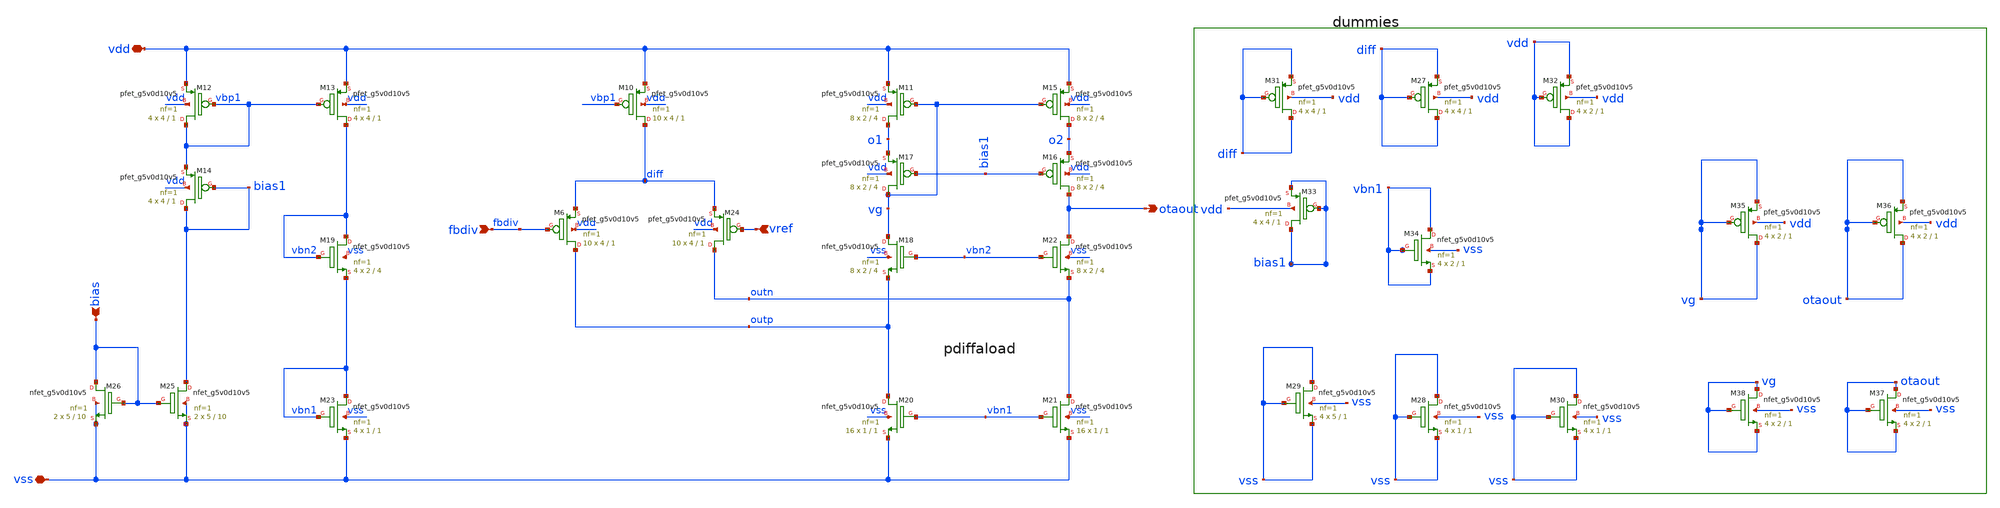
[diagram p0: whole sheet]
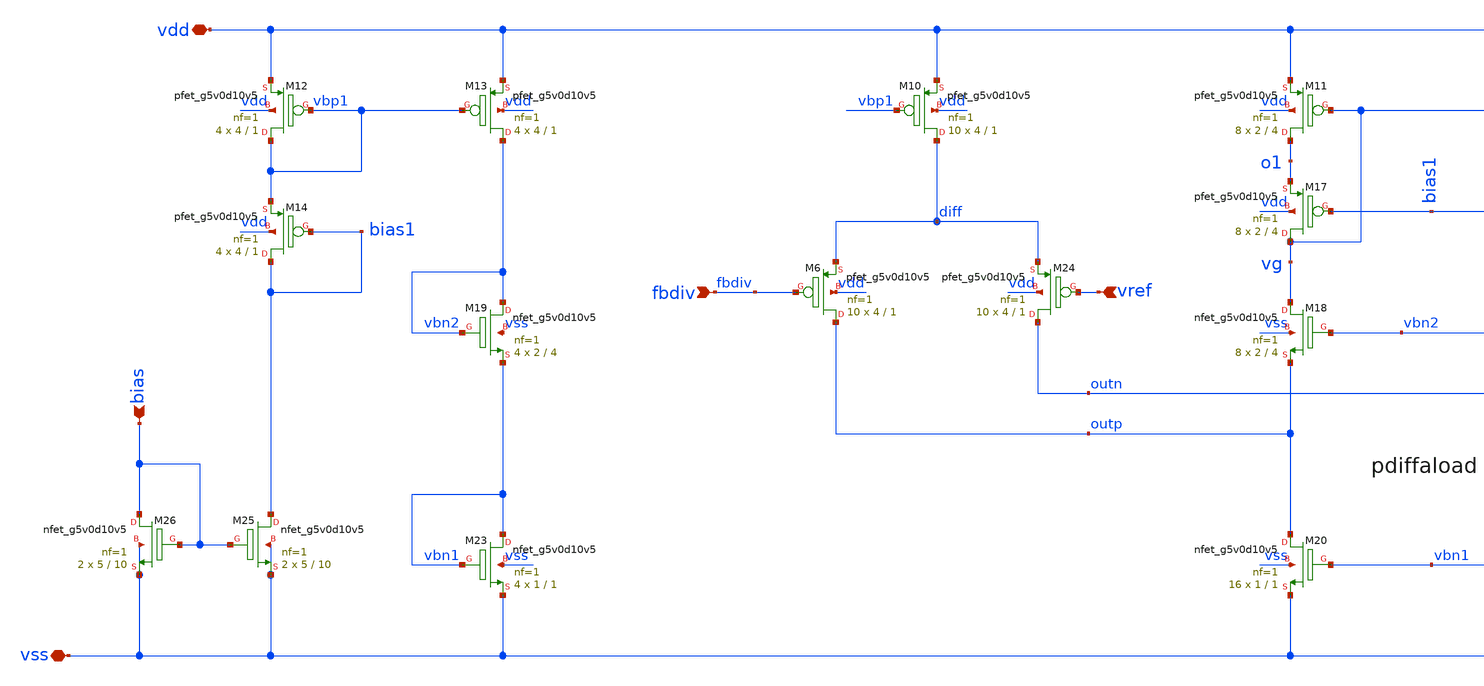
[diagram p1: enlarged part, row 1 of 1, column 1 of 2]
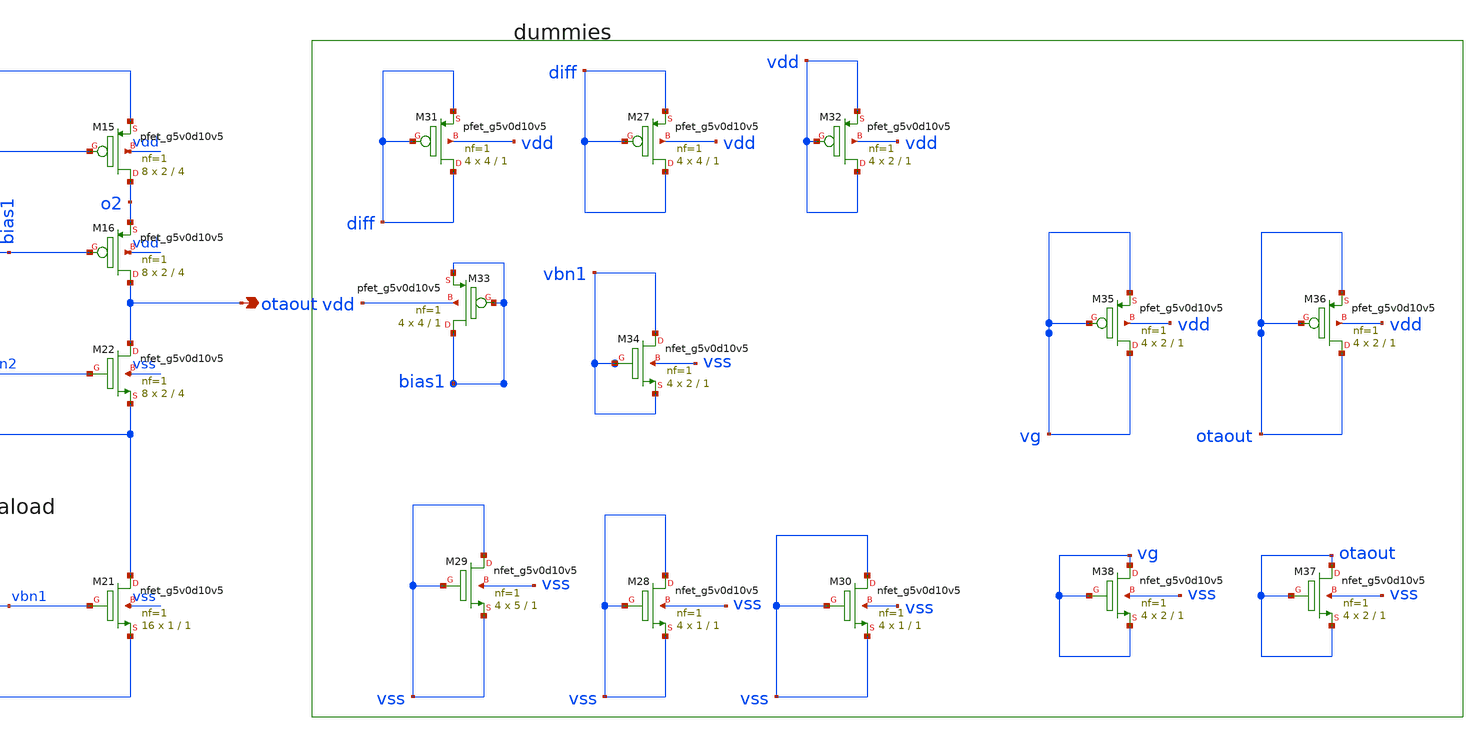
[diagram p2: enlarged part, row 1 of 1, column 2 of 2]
** sch_path: schematic/otaldox.sch
**.subckt otaldox vref bias vss vdd fbdiv otaout
*.ipin vref
*.ipin bias
*.iopin vss
*.iopin vdd
*.ipin fbdiv
*.opin otaout
XM12 vbp1 vbp1 vdd vdd sky130_fd_pr__pfet_g5v0d10v5 L=1 W=4 nf=1 ad='int((nf+1)/2) * W/nf * 0.29' as='int((nf+2)/2) * W/nf * 0.29'
+ pd='2*int((nf+1)/2) * (W/nf + 0.29)' ps='2*int((nf+2)/2) * (W/nf + 0.29)' nrd='0.29 / W' nrs='0.29 / W'
+ sa=0 sb=0 sd=0 mult=4 m=4
XM13 vbn2 vbp1 vdd vdd sky130_fd_pr__pfet_g5v0d10v5 L=1 W=4 nf=1 ad='int((nf+1)/2) * W/nf * 0.29' as='int((nf+2)/2) * W/nf * 0.29'
+ pd='2*int((nf+1)/2) * (W/nf + 0.29)' ps='2*int((nf+2)/2) * (W/nf + 0.29)' nrd='0.29 / W' nrs='0.29 / W'
+ sa=0 sb=0 sd=0 mult=4 m=4
XM14 bias1 bias1 vbp1 vdd sky130_fd_pr__pfet_g5v0d10v5 L=1 W=4 nf=1 ad='int((nf+1)/2) * W/nf * 0.29'
+ as='int((nf+2)/2) * W/nf * 0.29' pd='2*int((nf+1)/2) * (W/nf + 0.29)' ps='2*int((nf+2)/2) * (W/nf + 0.29)'
+ nrd='0.29 / W' nrs='0.29 / W' sa=0 sb=0 sd=0 mult=4 m=4
XM6 outp fbdiv diff vdd sky130_fd_pr__pfet_g5v0d10v5 L=1 W=4 nf=1 ad='int((nf+1)/2) * W/nf * 0.29' as='int((nf+2)/2) * W/nf * 0.29'
+ pd='2*int((nf+1)/2) * (W/nf + 0.29)' ps='2*int((nf+2)/2) * (W/nf + 0.29)' nrd='0.29 / W' nrs='0.29 / W'
+ sa=0 sb=0 sd=0 mult=10 m=10
XM10 diff vbp1 vdd vdd sky130_fd_pr__pfet_g5v0d10v5 L=1 W=4 nf=1 ad='int((nf+1)/2) * W/nf * 0.29' as='int((nf+2)/2) * W/nf * 0.29'
+ pd='2*int((nf+1)/2) * (W/nf + 0.29)' ps='2*int((nf+2)/2) * (W/nf + 0.29)' nrd='0.29 / W' nrs='0.29 / W'
+ sa=0 sb=0 sd=0 mult=10 m=10
XM11 o1 vg vdd vdd sky130_fd_pr__pfet_g5v0d10v5 L=4 W=2 nf=1 ad='int((nf+1)/2) * W/nf * 0.29' as='int((nf+2)/2) * W/nf * 0.29'
+ pd='2*int((nf+1)/2) * (W/nf + 0.29)' ps='2*int((nf+2)/2) * (W/nf + 0.29)' nrd='0.29 / W' nrs='0.29 / W'
+ sa=0 sb=0 sd=0 mult=8 m=8
XM15 o2 vg vdd vdd sky130_fd_pr__pfet_g5v0d10v5 L=4 W=2 nf=1 ad='int((nf+1)/2) * W/nf * 0.29' as='int((nf+2)/2) * W/nf * 0.29'
+ pd='2*int((nf+1)/2) * (W/nf + 0.29)' ps='2*int((nf+2)/2) * (W/nf + 0.29)' nrd='0.29 / W' nrs='0.29 / W'
+ sa=0 sb=0 sd=0 mult=8 m=8
XM16 otaout bias1 o2 vdd sky130_fd_pr__pfet_g5v0d10v5 L=4 W=2 nf=1 ad='int((nf+1)/2) * W/nf * 0.29' as='int((nf+2)/2) * W/nf * 0.29'
+ pd='2*int((nf+1)/2) * (W/nf + 0.29)' ps='2*int((nf+2)/2) * (W/nf + 0.29)' nrd='0.29 / W' nrs='0.29 / W'
+ sa=0 sb=0 sd=0 mult=8 m=8
XM17 vg bias1 o1 vdd sky130_fd_pr__pfet_g5v0d10v5 L=4 W=2 nf=1 ad='int((nf+1)/2) * W/nf * 0.29' as='int((nf+2)/2) * W/nf * 0.29'
+ pd='2*int((nf+1)/2) * (W/nf + 0.29)' ps='2*int((nf+2)/2) * (W/nf + 0.29)' nrd='0.29 / W' nrs='0.29 / W'
+ sa=0 sb=0 sd=0 mult=8 m=8
XM19 vbn2 vbn2 vbn1 vss sky130_fd_pr__nfet_g5v0d10v5 L=4 W=2 nf=1 ad='int((nf+1)/2) * W/nf * 0.29' as='int((nf+2)/2) * W/nf * 0.29'
+ pd='2*int((nf+1)/2) * (W/nf + 0.29)' ps='2*int((nf+2)/2) * (W/nf + 0.29)' nrd='0.29 / W' nrs='0.29 / W'
+ sa=0 sb=0 sd=0 mult=4 m=4
XM18 vg vbn2 outp vss sky130_fd_pr__nfet_g5v0d10v5 L=4 W=2 nf=1 ad='int((nf+1)/2) * W/nf * 0.29' as='int((nf+2)/2) * W/nf * 0.29'
+ pd='2*int((nf+1)/2) * (W/nf + 0.29)' ps='2*int((nf+2)/2) * (W/nf + 0.29)' nrd='0.29 / W' nrs='0.29 / W'
+ sa=0 sb=0 sd=0 mult=8 m=8
XM20 outp vbn1 vss vss sky130_fd_pr__nfet_g5v0d10v5 L=1 W=1 nf=1 ad='int((nf+1)/2) * W/nf * 0.29' as='int((nf+2)/2) * W/nf * 0.29'
+ pd='2*int((nf+1)/2) * (W/nf + 0.29)' ps='2*int((nf+2)/2) * (W/nf + 0.29)' nrd='0.29 / W' nrs='0.29 / W'
+ sa=0 sb=0 sd=0 mult=16 m=16
XM21 outn vbn1 vss vss sky130_fd_pr__nfet_g5v0d10v5 L=1 W=1 nf=1 ad='int((nf+1)/2) * W/nf * 0.29' as='int((nf+2)/2) * W/nf * 0.29'
+ pd='2*int((nf+1)/2) * (W/nf + 0.29)' ps='2*int((nf+2)/2) * (W/nf + 0.29)' nrd='0.29 / W' nrs='0.29 / W'
+ sa=0 sb=0 sd=0 mult=16 m=16
XM22 otaout vbn2 outn vss sky130_fd_pr__nfet_g5v0d10v5 L=4 W=2 nf=1 ad='int((nf+1)/2) * W/nf * 0.29'
+ as='int((nf+2)/2) * W/nf * 0.29' pd='2*int((nf+1)/2) * (W/nf + 0.29)' ps='2*int((nf+2)/2) * (W/nf + 0.29)'
+ nrd='0.29 / W' nrs='0.29 / W' sa=0 sb=0 sd=0 mult=8 m=8
XM23 vbn1 vbn1 vss vss sky130_fd_pr__nfet_g5v0d10v5 L=1 W=1 nf=1 ad='int((nf+1)/2) * W/nf * 0.29' as='int((nf+2)/2) * W/nf * 0.29'
+ pd='2*int((nf+1)/2) * (W/nf + 0.29)' ps='2*int((nf+2)/2) * (W/nf + 0.29)' nrd='0.29 / W' nrs='0.29 / W'
+ sa=0 sb=0 sd=0 mult=4 m=4
XM24 outn vref diff vdd sky130_fd_pr__pfet_g5v0d10v5 L=1 W=4 nf=1 ad='int((nf+1)/2) * W/nf * 0.29' as='int((nf+2)/2) * W/nf * 0.29'
+ pd='2*int((nf+1)/2) * (W/nf + 0.29)' ps='2*int((nf+2)/2) * (W/nf + 0.29)' nrd='0.29 / W' nrs='0.29 / W'
+ sa=0 sb=0 sd=0 mult=10 m=10
XM25 bias1 bias vss vss sky130_fd_pr__nfet_g5v0d10v5 L=10 W=5 nf=1 ad='int((nf+1)/2) * W/nf * 0.29' as='int((nf+2)/2) * W/nf * 0.29'
+ pd='2*int((nf+1)/2) * (W/nf + 0.29)' ps='2*int((nf+2)/2) * (W/nf + 0.29)' nrd='0.29 / W' nrs='0.29 / W'
+ sa=0 sb=0 sd=0 mult=2 m=2
XM26 bias bias vss vss sky130_fd_pr__nfet_g5v0d10v5 L=10 W=5 nf=1 ad='int((nf+1)/2) * W/nf * 0.29' as='int((nf+2)/2) * W/nf * 0.29'
+ pd='2*int((nf+1)/2) * (W/nf + 0.29)' ps='2*int((nf+2)/2) * (W/nf + 0.29)' nrd='0.29 / W' nrs='0.29 / W'
+ sa=0 sb=0 sd=0 mult=2 m=2
XM27 diff diff diff vdd sky130_fd_pr__pfet_g5v0d10v5 L=1 W=4 nf=1 ad='int((nf+1)/2) * W/nf * 0.29' as='int((nf+2)/2) * W/nf * 0.29'
+ pd='2*int((nf+1)/2) * (W/nf + 0.29)' ps='2*int((nf+2)/2) * (W/nf + 0.29)' nrd='0.29 / W' nrs='0.29 / W'
+ sa=0 sb=0 sd=0 mult=4 m=4
XM28 vss vss vss vss sky130_fd_pr__nfet_g5v0d10v5 L=1 W=1 nf=1 ad='int((nf+1)/2) * W/nf * 0.29' as='int((nf+2)/2) * W/nf * 0.29'
+ pd='2*int((nf+1)/2) * (W/nf + 0.29)' ps='2*int((nf+2)/2) * (W/nf + 0.29)' nrd='0.29 / W' nrs='0.29 / W'
+ sa=0 sb=0 sd=0 mult=4 m=4
XM29 vss vss vss vss sky130_fd_pr__nfet_g5v0d10v5 L=1 W=5 nf=1 ad='int((nf+1)/2) * W/nf * 0.29' as='int((nf+2)/2) * W/nf * 0.29'
+ pd='2*int((nf+1)/2) * (W/nf + 0.29)' ps='2*int((nf+2)/2) * (W/nf + 0.29)' nrd='0.29 / W' nrs='0.29 / W'
+ sa=0 sb=0 sd=0 mult=4 m=4
XM30 vss vss vss vss sky130_fd_pr__nfet_g5v0d10v5 L=1 W=1 nf=1 ad='int((nf+1)/2) * W/nf * 0.29' as='int((nf+2)/2) * W/nf * 0.29'
+ pd='2*int((nf+1)/2) * (W/nf + 0.29)' ps='2*int((nf+2)/2) * (W/nf + 0.29)' nrd='0.29 / W' nrs='0.29 / W'
+ sa=0 sb=0 sd=0 mult=4 m=4
XM31 diff diff diff vdd sky130_fd_pr__pfet_g5v0d10v5 L=1 W=4 nf=1 ad='int((nf+1)/2) * W/nf * 0.29' as='int((nf+2)/2) * W/nf * 0.29'
+ pd='2*int((nf+1)/2) * (W/nf + 0.29)' ps='2*int((nf+2)/2) * (W/nf + 0.29)' nrd='0.29 / W' nrs='0.29 / W'
+ sa=0 sb=0 sd=0 mult=4 m=4
XM32 vdd vdd vdd vdd sky130_fd_pr__pfet_g5v0d10v5 L=1 W=2 nf=1 ad='int((nf+1)/2) * W/nf * 0.29' as='int((nf+2)/2) * W/nf * 0.29'
+ pd='2*int((nf+1)/2) * (W/nf + 0.29)' ps='2*int((nf+2)/2) * (W/nf + 0.29)' nrd='0.29 / W' nrs='0.29 / W'
+ sa=0 sb=0 sd=0 mult=4 m=4
XM34 vbn1 vbn1 vbn1 vss sky130_fd_pr__nfet_g5v0d10v5 L=1 W=2 nf=1 ad='int((nf+1)/2) * W/nf * 0.29' as='int((nf+2)/2) * W/nf * 0.29'
+ pd='2*int((nf+1)/2) * (W/nf + 0.29)' ps='2*int((nf+2)/2) * (W/nf + 0.29)' nrd='0.29 / W' nrs='0.29 / W'
+ sa=0 sb=0 sd=0 mult=4 m=4
XM33 bias1 bias1 bias1 vdd sky130_fd_pr__pfet_g5v0d10v5 L=1 W=4 nf=1 ad='int((nf+1)/2) * W/nf * 0.29'
+ as='int((nf+2)/2) * W/nf * 0.29' pd='2*int((nf+1)/2) * (W/nf + 0.29)' ps='2*int((nf+2)/2) * (W/nf + 0.29)'
+ nrd='0.29 / W' nrs='0.29 / W' sa=0 sb=0 sd=0 mult=4 m=4
XM35 vg vg vg vdd sky130_fd_pr__pfet_g5v0d10v5 L=1 W=2 nf=1 ad='int((nf+1)/2) * W/nf * 0.29' as='int((nf+2)/2) * W/nf * 0.29'
+ pd='2*int((nf+1)/2) * (W/nf + 0.29)' ps='2*int((nf+2)/2) * (W/nf + 0.29)' nrd='0.29 / W' nrs='0.29 / W'
+ sa=0 sb=0 sd=0 mult=4 m=4
XM36 otaout otaout otaout vdd sky130_fd_pr__pfet_g5v0d10v5 L=1 W=2 nf=1 ad='int((nf+1)/2) * W/nf * 0.29'
+ as='int((nf+2)/2) * W/nf * 0.29' pd='2*int((nf+1)/2) * (W/nf + 0.29)' ps='2*int((nf+2)/2) * (W/nf + 0.29)'
+ nrd='0.29 / W' nrs='0.29 / W' sa=0 sb=0 sd=0 mult=4 m=4
XM37 otaout otaout otaout vss sky130_fd_pr__nfet_g5v0d10v5 L=1 W=2 nf=1 ad='int((nf+1)/2) * W/nf * 0.29'
+ as='int((nf+2)/2) * W/nf * 0.29' pd='2*int((nf+1)/2) * (W/nf + 0.29)' ps='2*int((nf+2)/2) * (W/nf + 0.29)'
+ nrd='0.29 / W' nrs='0.29 / W' sa=0 sb=0 sd=0 mult=4 m=4
XM38 vg vg vg vss sky130_fd_pr__nfet_g5v0d10v5 L=1 W=2 nf=1 ad='int((nf+1)/2) * W/nf * 0.29' as='int((nf+2)/2) * W/nf * 0.29'
+ pd='2*int((nf+1)/2) * (W/nf + 0.29)' ps='2*int((nf+2)/2) * (W/nf + 0.29)' nrd='0.29 / W' nrs='0.29 / W'
+ sa=0 sb=0 sd=0 mult=4 m=4
**.ends
.end
